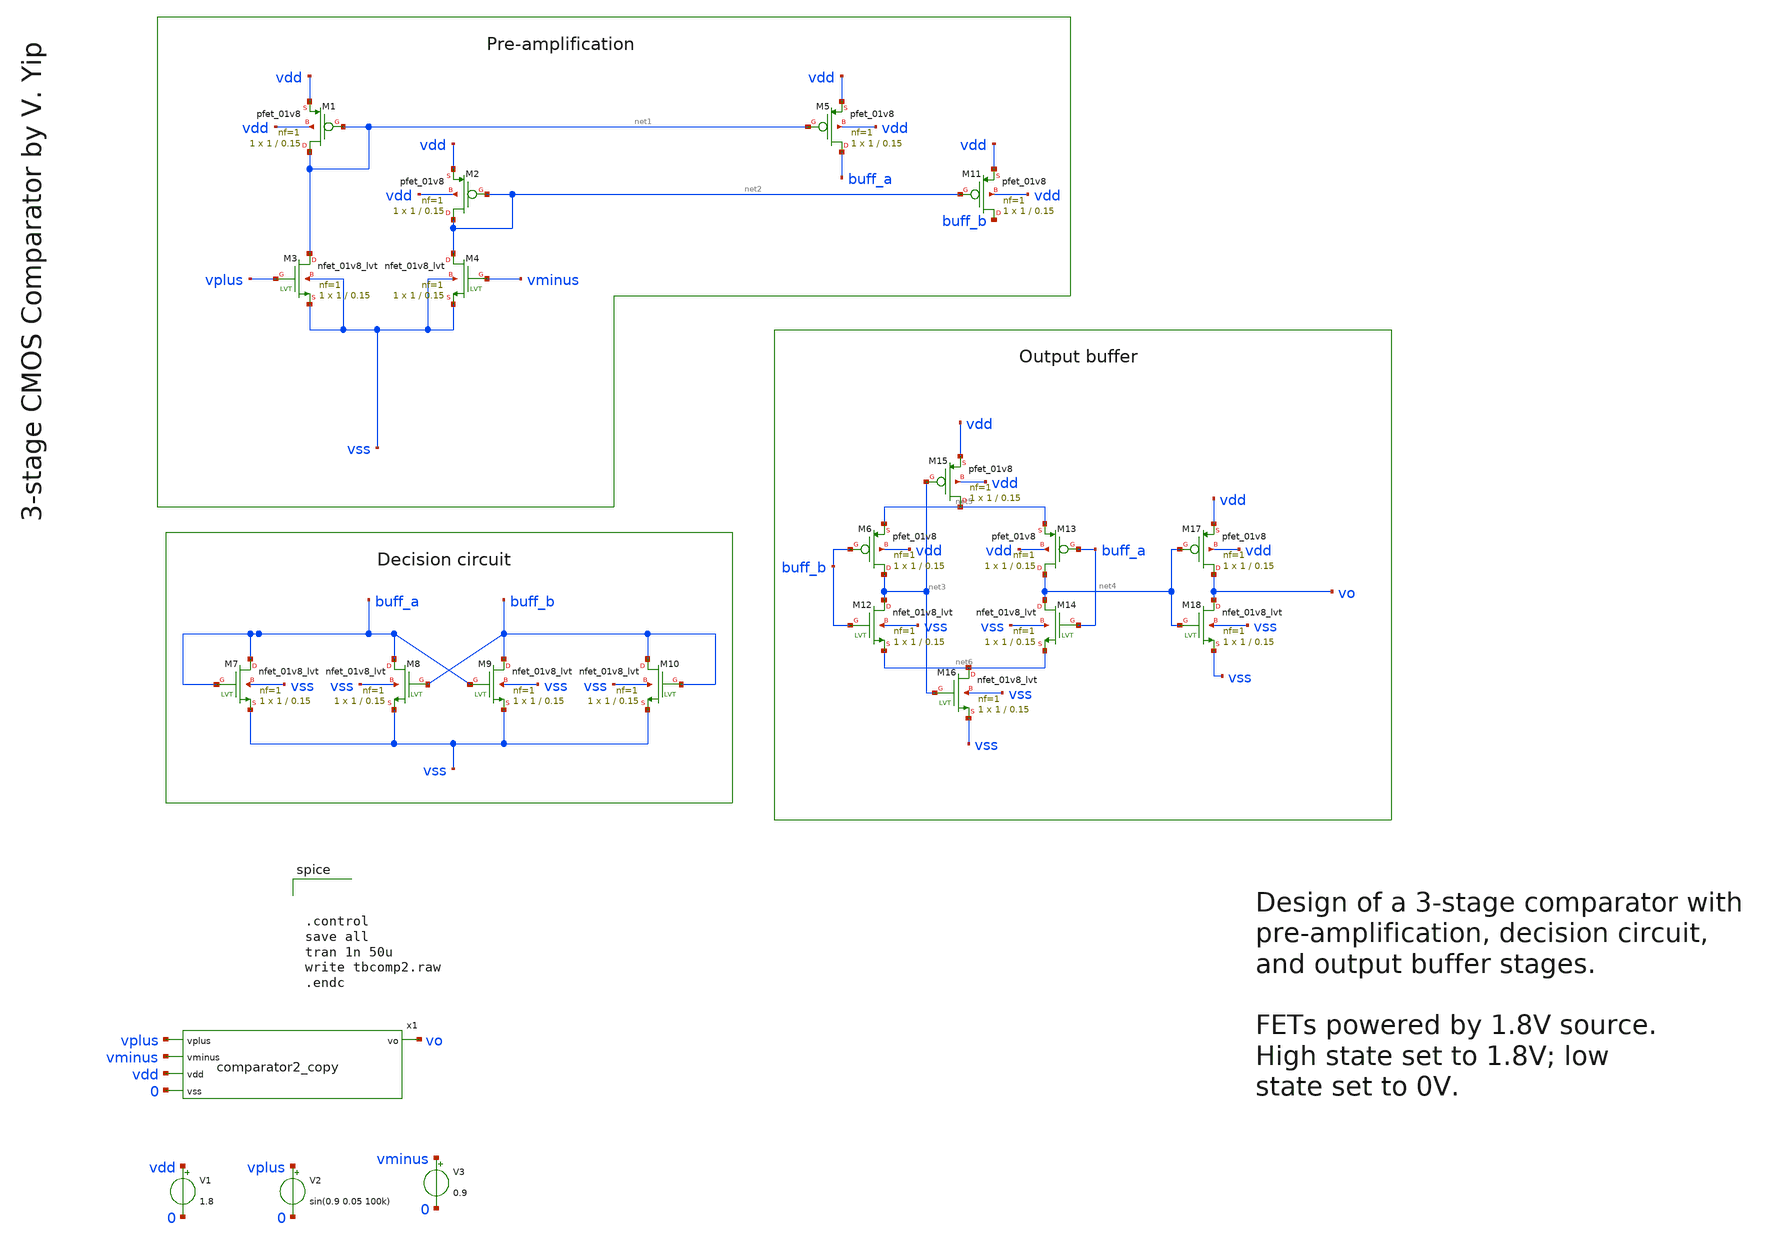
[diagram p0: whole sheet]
** sch_path: frontpage.sch
**.subckt frontpage
V1 vdd 0 1.8
V2 vplus 0 sin(0.9 0.05 100k)
V3 vminus 0 0.9
XM1 net1 net1 vdd vdd sky130_fd_pr__pfet_01v8 L=0.15 W=1 nf=1 ad='int((1 + 1)/2) * 1 / 1 * 0.29' as='int((1 + 2)/2) * 1 / 1 * 0.29'
+ pd='2*int((1 + 1)/2) * (1 / 1 + 0.29)' ps='2*int((1 + 2)/2) * (1 / 1 + 0.29)' nrd='0.29 / 1 ' nrs='0.29 / 1 '
+ sa=0 sb=0 sd=0 mult=1 m=1
XM2 net2 net2 vdd vdd sky130_fd_pr__pfet_01v8 L=0.15 W=1 nf=1 ad='int((1 + 1)/2) * 1 / 1 * 0.29' as='int((1 + 2)/2) * 1 / 1 * 0.29'
+ pd='2*int((1 + 1)/2) * (1 / 1 + 0.29)' ps='2*int((1 + 2)/2) * (1 / 1 + 0.29)' nrd='0.29 / 1 ' nrs='0.29 / 1 '
+ sa=0 sb=0 sd=0 mult=1 m=1
XM3 net1 vplus vss vss sky130_fd_pr__nfet_01v8_lvt L=0.15 W=1 nf=1 ad='int((1 + 1)/2) * 1 / 1 * 0.29'
+ as='int((1 + 2)/2) * 1 / 1 * 0.29' pd='2*int((1 + 1)/2) * (1 / 1 + 0.29)' ps='2*int((1 + 2)/2) * (1 / 1 + 0.29)'
+ nrd='0.29 / 1 ' nrs='0.29 / 1 ' sa=0 sb=0 sd=0 mult=1 m=1
XM4 net2 vminus vss vss sky130_fd_pr__nfet_01v8_lvt L=0.15 W=1 nf=1 ad='int((1 + 1)/2) * 1 / 1 * 0.29'
+ as='int((1 + 2)/2) * 1 / 1 * 0.29' pd='2*int((1 + 1)/2) * (1 / 1 + 0.29)' ps='2*int((1 + 2)/2) * (1 / 1 + 0.29)'
+ nrd='0.29 / 1 ' nrs='0.29 / 1 ' sa=0 sb=0 sd=0 mult=1 m=1
XM5 buff_a net1 vdd vdd sky130_fd_pr__pfet_01v8 L=0.15 W=1 nf=1 ad='int((1 + 1)/2) * 1 / 1 * 0.29' as='int((1 + 2)/2) * 1 / 1 * 0.29'
+ pd='2*int((1 + 1)/2) * (1 / 1 + 0.29)' ps='2*int((1 + 2)/2) * (1 / 1 + 0.29)' nrd='0.29 / 1 ' nrs='0.29 / 1 '
+ sa=0 sb=0 sd=0 mult=1 m=1
XM7 buff_a buff_a vss vss sky130_fd_pr__nfet_01v8_lvt L=0.15 W=1 nf=1 ad='int((1 + 1)/2) * 1 / 1 * 0.29'
+ as='int((1 + 2)/2) * 1 / 1 * 0.29' pd='2*int((1 + 1)/2) * (1 / 1 + 0.29)' ps='2*int((1 + 2)/2) * (1 / 1 + 0.29)'
+ nrd='0.29 / 1 ' nrs='0.29 / 1 ' sa=0 sb=0 sd=0 mult=1 m=1
XM8 buff_a buff_b vss vss sky130_fd_pr__nfet_01v8_lvt L=0.15 W=1 nf=1 ad='int((1 + 1)/2) * 1 / 1 * 0.29'
+ as='int((1 + 2)/2) * 1 / 1 * 0.29' pd='2*int((1 + 1)/2) * (1 / 1 + 0.29)' ps='2*int((1 + 2)/2) * (1 / 1 + 0.29)'
+ nrd='0.29 / 1 ' nrs='0.29 / 1 ' sa=0 sb=0 sd=0 mult=1 m=1
XM9 buff_b buff_a vss vss sky130_fd_pr__nfet_01v8_lvt L=0.15 W=1 nf=1 ad='int((1 + 1)/2) * 1 / 1 * 0.29'
+ as='int((1 + 2)/2) * 1 / 1 * 0.29' pd='2*int((1 + 1)/2) * (1 / 1 + 0.29)' ps='2*int((1 + 2)/2) * (1 / 1 + 0.29)'
+ nrd='0.29 / 1 ' nrs='0.29 / 1 ' sa=0 sb=0 sd=0 mult=1 m=1
XM10 buff_b buff_b vss vss sky130_fd_pr__nfet_01v8_lvt L=0.15 W=1 nf=1 ad='int((1 + 1)/2) * 1 / 1 * 0.29'
+ as='int((1 + 2)/2) * 1 / 1 * 0.29' pd='2*int((1 + 1)/2) * (1 / 1 + 0.29)' ps='2*int((1 + 2)/2) * (1 / 1 + 0.29)'
+ nrd='0.29 / 1 ' nrs='0.29 / 1 ' sa=0 sb=0 sd=0 mult=1 m=1
XM11 buff_b net2 vdd vdd sky130_fd_pr__pfet_01v8 L=0.15 W=1 nf=1 ad='int((1 + 1)/2) * 1 / 1 * 0.29' as='int((1 + 2)/2) * 1 / 1 * 0.29'
+ pd='2*int((1 + 1)/2) * (1 / 1 + 0.29)' ps='2*int((1 + 2)/2) * (1 / 1 + 0.29)' nrd='0.29 / 1 ' nrs='0.29 / 1 '
+ sa=0 sb=0 sd=0 mult=1 m=1
XM6 net3 buff_b net5 vdd sky130_fd_pr__pfet_01v8 L=0.15 W=1 nf=1 ad='int((1 + 1)/2) * 1 / 1 * 0.29' as='int((1 + 2)/2) * 1 / 1 * 0.29'
+ pd='2*int((1 + 1)/2) * (1 / 1 + 0.29)' ps='2*int((1 + 2)/2) * (1 / 1 + 0.29)' nrd='0.29 / 1 ' nrs='0.29 / 1 '
+ sa=0 sb=0 sd=0 mult=1 m=1
XM12 net3 buff_b net6 vss sky130_fd_pr__nfet_01v8_lvt L=0.15 W=1 nf=1 ad='int((1 + 1)/2) * 1 / 1 * 0.29'
+ as='int((1 + 2)/2) * 1 / 1 * 0.29' pd='2*int((1 + 1)/2) * (1 / 1 + 0.29)' ps='2*int((1 + 2)/2) * (1 / 1 + 0.29)'
+ nrd='0.29 / 1 ' nrs='0.29 / 1 ' sa=0 sb=0 sd=0 mult=1 m=1
XM13 net4 buff_a net5 vdd sky130_fd_pr__pfet_01v8 L=0.15 W=1 nf=1 ad='int((1 + 1)/2) * 1 / 1 * 0.29'
+ as='int((1 + 2)/2) * 1 / 1 * 0.29' pd='2*int((1 + 1)/2) * (1 / 1 + 0.29)' ps='2*int((1 + 2)/2) * (1 / 1 + 0.29)'
+ nrd='0.29 / 1 ' nrs='0.29 / 1 ' sa=0 sb=0 sd=0 mult=1 m=1
XM14 net4 buff_a net6 vss sky130_fd_pr__nfet_01v8_lvt L=0.15 W=1 nf=1 ad='int((1 + 1)/2) * 1 / 1 * 0.29'
+ as='int((1 + 2)/2) * 1 / 1 * 0.29' pd='2*int((1 + 1)/2) * (1 / 1 + 0.29)' ps='2*int((1 + 2)/2) * (1 / 1 + 0.29)'
+ nrd='0.29 / 1 ' nrs='0.29 / 1 ' sa=0 sb=0 sd=0 mult=1 m=1
XM15 net5 net3 vdd vdd sky130_fd_pr__pfet_01v8 L=0.15 W=1 nf=1 ad='int((1 + 1)/2) * 1 / 1 * 0.29' as='int((1 + 2)/2) * 1 / 1 * 0.29'
+ pd='2*int((1 + 1)/2) * (1 / 1 + 0.29)' ps='2*int((1 + 2)/2) * (1 / 1 + 0.29)' nrd='0.29 / 1 ' nrs='0.29 / 1 '
+ sa=0 sb=0 sd=0 mult=1 m=1
XM16 net6 net3 vss vss sky130_fd_pr__nfet_01v8_lvt L=0.15 W=1 nf=1 ad='int((1 + 1)/2) * 1 / 1 * 0.29'
+ as='int((1 + 2)/2) * 1 / 1 * 0.29' pd='2*int((1 + 1)/2) * (1 / 1 + 0.29)' ps='2*int((1 + 2)/2) * (1 / 1 + 0.29)'
+ nrd='0.29 / 1 ' nrs='0.29 / 1 ' sa=0 sb=0 sd=0 mult=1 m=1
XM17 vo net4 vdd vdd sky130_fd_pr__pfet_01v8 L=0.15 W=1 nf=1 ad='int((1 + 1)/2) * 1 / 1 * 0.29' as='int((1 + 2)/2) * 1 / 1 * 0.29'
+ pd='2*int((1 + 1)/2) * (1 / 1 + 0.29)' ps='2*int((1 + 2)/2) * (1 / 1 + 0.29)' nrd='0.29 / 1 ' nrs='0.29 / 1 '
+ sa=0 sb=0 sd=0 mult=1 m=1
XM18 vo net4 vss vss sky130_fd_pr__nfet_01v8_lvt L=0.15 W=1 nf=1 ad='int((1 + 1)/2) * 1 / 1 * 0.29' as='int((1 + 2)/2) * 1 / 1 * 0.29'
+ pd='2*int((1 + 1)/2) * (1 / 1 + 0.29)' ps='2*int((1 + 2)/2) * (1 / 1 + 0.29)' nrd='0.29 / 1 ' nrs='0.29 / 1 '
+ sa=0 sb=0 sd=0 mult=1 m=1
x1 vo vplus vminus vdd 0 comparator2_copy
**** begin user architecture code
 .lib /usr/local/share/pdk/sky130A/libs.tech/combined/sky130.lib.spice tt



.control
save all
tran 1n 50u
write tbcomp2.raw
.endc


**** end user architecture code
**.ends

* expanding   symbol:  /home/valerie/projects/comp2_git/comparator2_copy.sym # of pins=5
** sym_path: comparator2_copy.sym
** sch_path: comparator2_copy.sch
.subckt comparator2_copy vo vplus vminus vdd vss
*.ipin vplus
*.ipin vminus
*.ipin vdd
*.ipin vss
*.opin vo
XM1 net1 net1 vdd vdd sky130_fd_pr__pfet_01v8 L=0.15 W=1 nf=1 ad='int((1 + 1)/2) * 1 / 1 * 0.29' as='int((1 + 2)/2) * 1 / 1 * 0.29'
+ pd='2*int((1 + 1)/2) * (1 / 1 + 0.29)' ps='2*int((1 + 2)/2) * (1 / 1 + 0.29)' nrd='0.29 / 1 ' nrs='0.29 / 1 '
+ sa=0 sb=0 sd=0 mult=1 m=1
XM2 net2 net2 vdd vdd sky130_fd_pr__pfet_01v8 L=0.15 W=1 nf=1 ad='int((1 + 1)/2) * 1 / 1 * 0.29' as='int((1 + 2)/2) * 1 / 1 * 0.29'
+ pd='2*int((1 + 1)/2) * (1 / 1 + 0.29)' ps='2*int((1 + 2)/2) * (1 / 1 + 0.29)' nrd='0.29 / 1 ' nrs='0.29 / 1 '
+ sa=0 sb=0 sd=0 mult=1 m=1
XM3 net1 vplus vss vss sky130_fd_pr__nfet_01v8_lvt L=0.15 W=1 nf=1 ad='int((1 + 1)/2) * 1 / 1 * 0.29'
+ as='int((1 + 2)/2) * 1 / 1 * 0.29' pd='2*int((1 + 1)/2) * (1 / 1 + 0.29)' ps='2*int((1 + 2)/2) * (1 / 1 + 0.29)'
+ nrd='0.29 / 1 ' nrs='0.29 / 1 ' sa=0 sb=0 sd=0 mult=1 m=1
XM4 net2 vminus vss vss sky130_fd_pr__nfet_01v8_lvt L=0.15 W=1 nf=1 ad='int((1 + 1)/2) * 1 / 1 * 0.29'
+ as='int((1 + 2)/2) * 1 / 1 * 0.29' pd='2*int((1 + 1)/2) * (1 / 1 + 0.29)' ps='2*int((1 + 2)/2) * (1 / 1 + 0.29)'
+ nrd='0.29 / 1 ' nrs='0.29 / 1 ' sa=0 sb=0 sd=0 mult=1 m=1
XM5 buff_a net1 vdd vdd sky130_fd_pr__pfet_01v8 L=0.15 W=1 nf=1 ad='int((1 + 1)/2) * 1 / 1 * 0.29' as='int((1 + 2)/2) * 1 / 1 * 0.29'
+ pd='2*int((1 + 1)/2) * (1 / 1 + 0.29)' ps='2*int((1 + 2)/2) * (1 / 1 + 0.29)' nrd='0.29 / 1 ' nrs='0.29 / 1 '
+ sa=0 sb=0 sd=0 mult=1 m=1
XM7 buff_a buff_a vss vss sky130_fd_pr__nfet_01v8_lvt L=0.15 W=1 nf=1 ad='int((1 + 1)/2) * 1 / 1 * 0.29'
+ as='int((1 + 2)/2) * 1 / 1 * 0.29' pd='2*int((1 + 1)/2) * (1 / 1 + 0.29)' ps='2*int((1 + 2)/2) * (1 / 1 + 0.29)'
+ nrd='0.29 / 1 ' nrs='0.29 / 1 ' sa=0 sb=0 sd=0 mult=1 m=1
XM8 buff_a buff_b vss vss sky130_fd_pr__nfet_01v8_lvt L=0.15 W=1 nf=1 ad='int((1 + 1)/2) * 1 / 1 * 0.29'
+ as='int((1 + 2)/2) * 1 / 1 * 0.29' pd='2*int((1 + 1)/2) * (1 / 1 + 0.29)' ps='2*int((1 + 2)/2) * (1 / 1 + 0.29)'
+ nrd='0.29 / 1 ' nrs='0.29 / 1 ' sa=0 sb=0 sd=0 mult=1 m=1
XM9 buff_b buff_a vss vss sky130_fd_pr__nfet_01v8_lvt L=0.15 W=1 nf=1 ad='int((1 + 1)/2) * 1 / 1 * 0.29'
+ as='int((1 + 2)/2) * 1 / 1 * 0.29' pd='2*int((1 + 1)/2) * (1 / 1 + 0.29)' ps='2*int((1 + 2)/2) * (1 / 1 + 0.29)'
+ nrd='0.29 / 1 ' nrs='0.29 / 1 ' sa=0 sb=0 sd=0 mult=1 m=1
XM10 buff_b buff_b vss vss sky130_fd_pr__nfet_01v8_lvt L=0.15 W=1 nf=1 ad='int((1 + 1)/2) * 1 / 1 * 0.29'
+ as='int((1 + 2)/2) * 1 / 1 * 0.29' pd='2*int((1 + 1)/2) * (1 / 1 + 0.29)' ps='2*int((1 + 2)/2) * (1 / 1 + 0.29)'
+ nrd='0.29 / 1 ' nrs='0.29 / 1 ' sa=0 sb=0 sd=0 mult=1 m=1
XM11 buff_b net2 vdd vdd sky130_fd_pr__pfet_01v8 L=0.15 W=1 nf=1 ad='int((1 + 1)/2) * 1 / 1 * 0.29' as='int((1 + 2)/2) * 1 / 1 * 0.29'
+ pd='2*int((1 + 1)/2) * (1 / 1 + 0.29)' ps='2*int((1 + 2)/2) * (1 / 1 + 0.29)' nrd='0.29 / 1 ' nrs='0.29 / 1 '
+ sa=0 sb=0 sd=0 mult=1 m=1
XM6 net3 buff_b net5 vdd sky130_fd_pr__pfet_01v8 L=0.15 W=1 nf=1 ad='int((1 + 1)/2) * 1 / 1 * 0.29' as='int((1 + 2)/2) * 1 / 1 * 0.29'
+ pd='2*int((1 + 1)/2) * (1 / 1 + 0.29)' ps='2*int((1 + 2)/2) * (1 / 1 + 0.29)' nrd='0.29 / 1 ' nrs='0.29 / 1 '
+ sa=0 sb=0 sd=0 mult=1 m=1
XM12 net3 buff_b net6 vss sky130_fd_pr__nfet_01v8_lvt L=0.15 W=1 nf=1 ad='int((1 + 1)/2) * 1 / 1 * 0.29'
+ as='int((1 + 2)/2) * 1 / 1 * 0.29' pd='2*int((1 + 1)/2) * (1 / 1 + 0.29)' ps='2*int((1 + 2)/2) * (1 / 1 + 0.29)'
+ nrd='0.29 / 1 ' nrs='0.29 / 1 ' sa=0 sb=0 sd=0 mult=1 m=1
XM13 net4 buff_a net5 vdd sky130_fd_pr__pfet_01v8 L=0.15 W=1 nf=1 ad='int((1 + 1)/2) * 1 / 1 * 0.29'
+ as='int((1 + 2)/2) * 1 / 1 * 0.29' pd='2*int((1 + 1)/2) * (1 / 1 + 0.29)' ps='2*int((1 + 2)/2) * (1 / 1 + 0.29)'
+ nrd='0.29 / 1 ' nrs='0.29 / 1 ' sa=0 sb=0 sd=0 mult=1 m=1
XM14 net4 buff_a net6 vss sky130_fd_pr__nfet_01v8_lvt L=0.15 W=1 nf=1 ad='int((1 + 1)/2) * 1 / 1 * 0.29'
+ as='int((1 + 2)/2) * 1 / 1 * 0.29' pd='2*int((1 + 1)/2) * (1 / 1 + 0.29)' ps='2*int((1 + 2)/2) * (1 / 1 + 0.29)'
+ nrd='0.29 / 1 ' nrs='0.29 / 1 ' sa=0 sb=0 sd=0 mult=1 m=1
XM15 net5 net3 vdd vdd sky130_fd_pr__pfet_01v8 L=0.15 W=1 nf=1 ad='int((1 + 1)/2) * 1 / 1 * 0.29' as='int((1 + 2)/2) * 1 / 1 * 0.29'
+ pd='2*int((1 + 1)/2) * (1 / 1 + 0.29)' ps='2*int((1 + 2)/2) * (1 / 1 + 0.29)' nrd='0.29 / 1 ' nrs='0.29 / 1 '
+ sa=0 sb=0 sd=0 mult=1 m=1
XM16 net6 net3 vss vss sky130_fd_pr__nfet_01v8_lvt L=0.15 W=1 nf=1 ad='int((1 + 1)/2) * 1 / 1 * 0.29'
+ as='int((1 + 2)/2) * 1 / 1 * 0.29' pd='2*int((1 + 1)/2) * (1 / 1 + 0.29)' ps='2*int((1 + 2)/2) * (1 / 1 + 0.29)'
+ nrd='0.29 / 1 ' nrs='0.29 / 1 ' sa=0 sb=0 sd=0 mult=1 m=1
XM17 vo net4 vdd vdd sky130_fd_pr__pfet_01v8 L=0.15 W=1 nf=1 ad='int((1 + 1)/2) * 1 / 1 * 0.29' as='int((1 + 2)/2) * 1 / 1 * 0.29'
+ pd='2*int((1 + 1)/2) * (1 / 1 + 0.29)' ps='2*int((1 + 2)/2) * (1 / 1 + 0.29)' nrd='0.29 / 1 ' nrs='0.29 / 1 '
+ sa=0 sb=0 sd=0 mult=1 m=1
XM18 vo net4 vss vss sky130_fd_pr__nfet_01v8_lvt L=0.15 W=1 nf=1 ad='int((1 + 1)/2) * 1 / 1 * 0.29' as='int((1 + 2)/2) * 1 / 1 * 0.29'
+ pd='2*int((1 + 1)/2) * (1 / 1 + 0.29)' ps='2*int((1 + 2)/2) * (1 / 1 + 0.29)' nrd='0.29 / 1 ' nrs='0.29 / 1 '
+ sa=0 sb=0 sd=0 mult=1 m=1
.ends

.end
